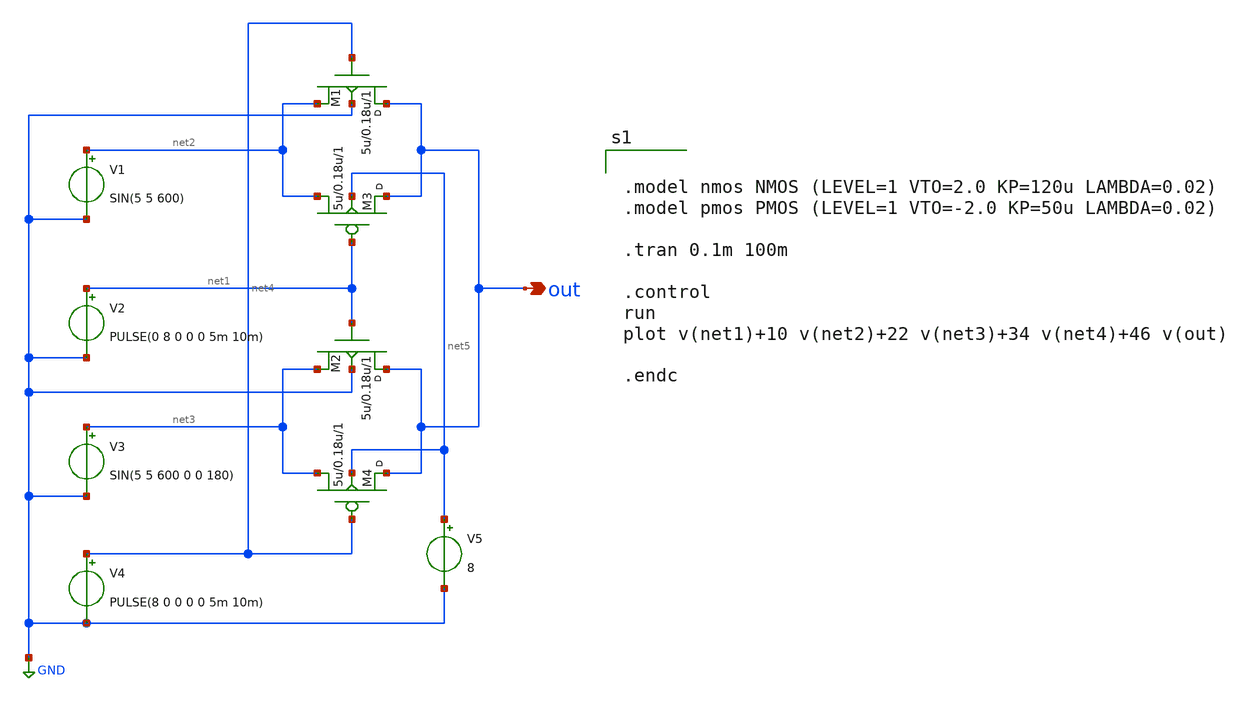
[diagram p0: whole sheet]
** sch_path: Xschem Files/analog_mux_bpsk.sch
**.subckt analog_mux_bpsk out
*.opin out
V1 net2 GND SIN(5 5 600)
V2 net1 GND PULSE(0 8 0 0 0 5m 10m)
V3 net3 GND SIN(5 5 600 0 0 180)
V4 net4 GND PULSE(8 0 0 0 0 5m 10m)
M1 out net4 net2 GND nmos w=5u l=0.18u m=1
M2 out net1 net3 GND nmos w=5u l=0.18u m=1
M3 out net1 net2 net5 pmos w=5u l=0.18u m=1
M4 out net4 net3 net5 pmos w=5u l=0.18u m=1
V5 net5 GND 8
**** begin user architecture code


.model nmos NMOS (LEVEL=1 VTO=2.0 KP=120u LAMBDA=0.02)
.model pmos PMOS (LEVEL=1 VTO=-2.0 KP=50u LAMBDA=0.02)

.tran 0.1m 100m

.control
run
plot v(net1)+10 v(net2)+22 v(net3)+34 v(net4)+46 v(out)

.endc


**** end user architecture code
**.ends
.GLOBAL GND
.end
